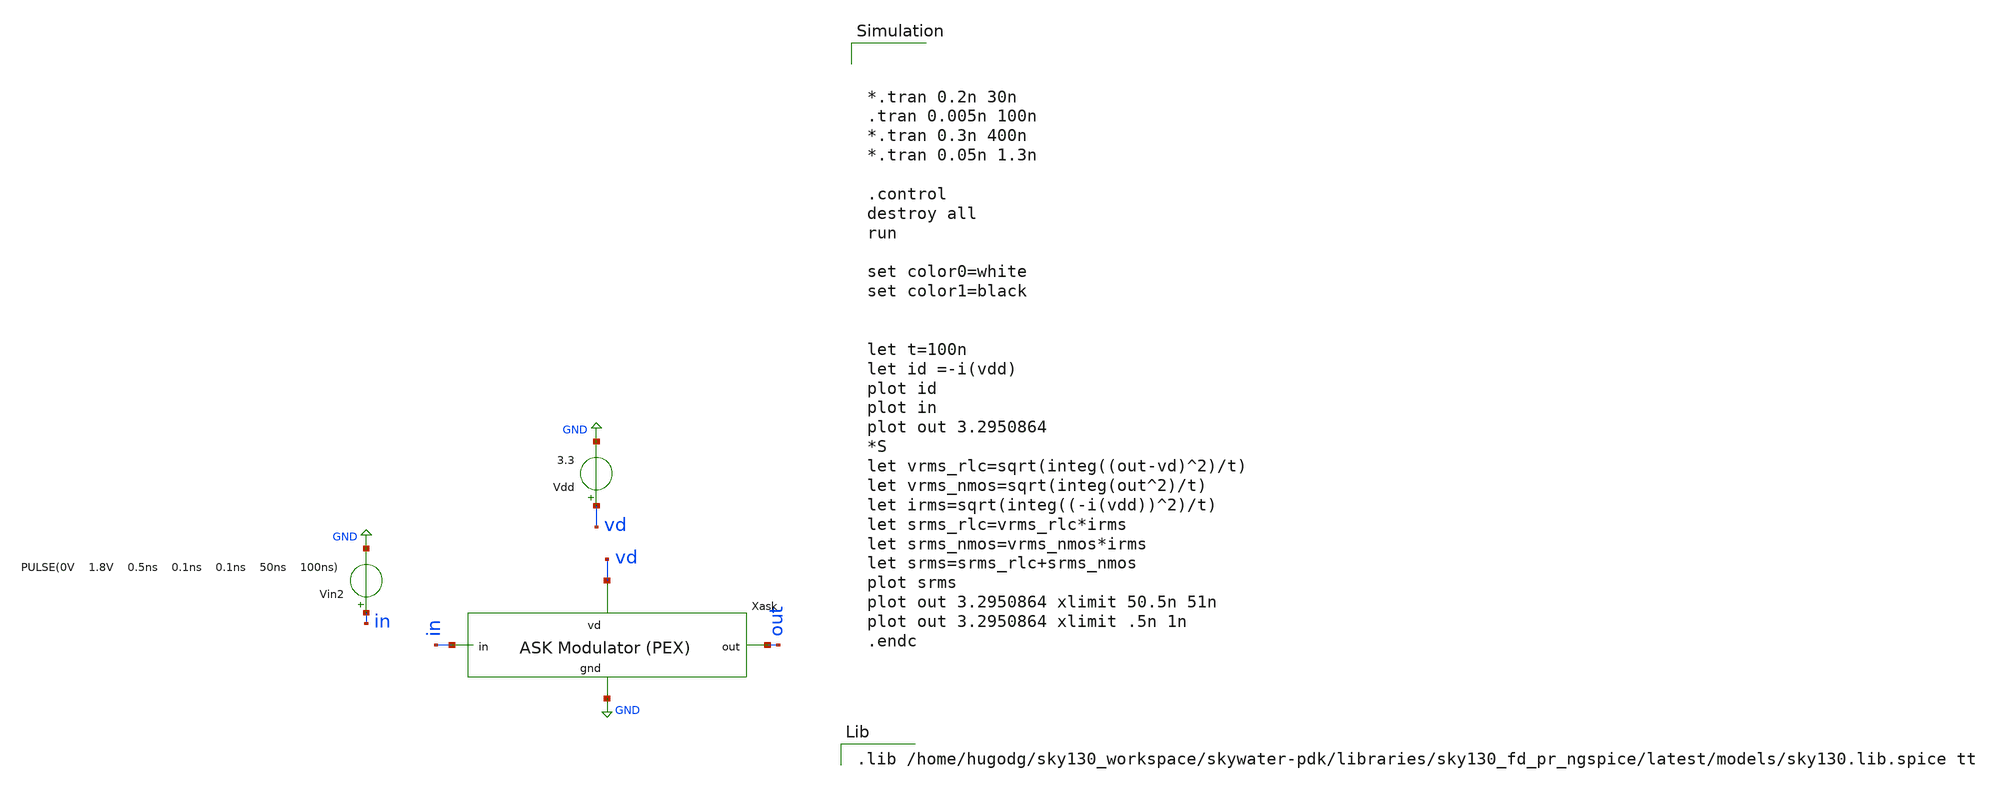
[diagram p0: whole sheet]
** sch_path: ask_modulator/xschem/ask-modulator-pex_tb-tran.sch
**.subckt ask-modulator-pex_tb-tran
Vdd vd GND 3.3
Vin2 in GND PULSE(0V 1.8V 0.5ns 0.1ns 0.1ns 50ns 100ns)
x1 vd out in GND ask-modulator-pex
**** begin user architecture code



*.tran 0.2n 30n
.tran 0.005n 100n
*.tran 0.3n 400n
*.tran 0.05n 1.3n

.control
destroy all
run

set color0=white
set color1=black


let t=100n
let id =-i(vdd)
plot id
plot in
plot out 3.2950864
*S
let vrms_rlc=sqrt(integ((out-vd)^2)/t)
let vrms_nmos=sqrt(integ(out^2)/t)
let irms=sqrt(integ((-i(vdd))^2)/t)
let srms_rlc=vrms_rlc*irms
let srms_nmos=vrms_nmos*irms
let srms=srms_rlc+srms_nmos
plot srms
plot out 3.2950864 xlimit 50.5n 51n
plot out 3.2950864 xlimit .5n 1n
.endc


.lib /home/hugodg/sky130_workspace/skywater-pdk/libraries/sky130_fd_pr_ngspice/latest/models/sky130.lib.spice tt

**** end user architecture code
**.ends
.GLOBAL GND
.end
